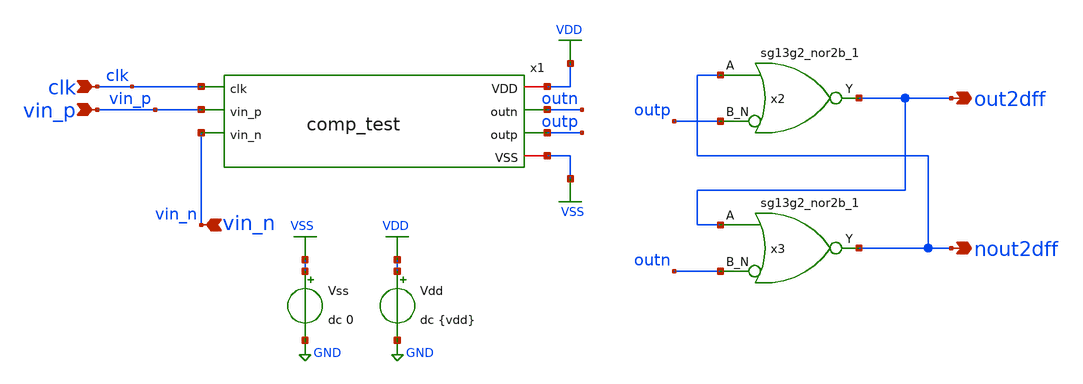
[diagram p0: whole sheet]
** sch_path: DSM/Schematics/new_comp/final_working_comp.sch
**.subckt final_working_comp out2dff nout2dff clk vin_p vin_n
*.opin out2dff
*.opin nout2dff
*.ipin clk
*.ipin vin_p
*.ipin vin_n
Vdd VDD GND dc {vdd}
Vss VSS GND dc 0
x2 out2dff nout2dff outp VDD VSS sg13g2_nor2b_1
x3 nout2dff out2dff outn VDD VSS sg13g2_nor2b_1
x1 VDD clk outn outp vin_p vin_n VSS comp_test
**.ends
.GLOBAL GND
.GLOBAL VDD
.GLOBAL VSS
.end
